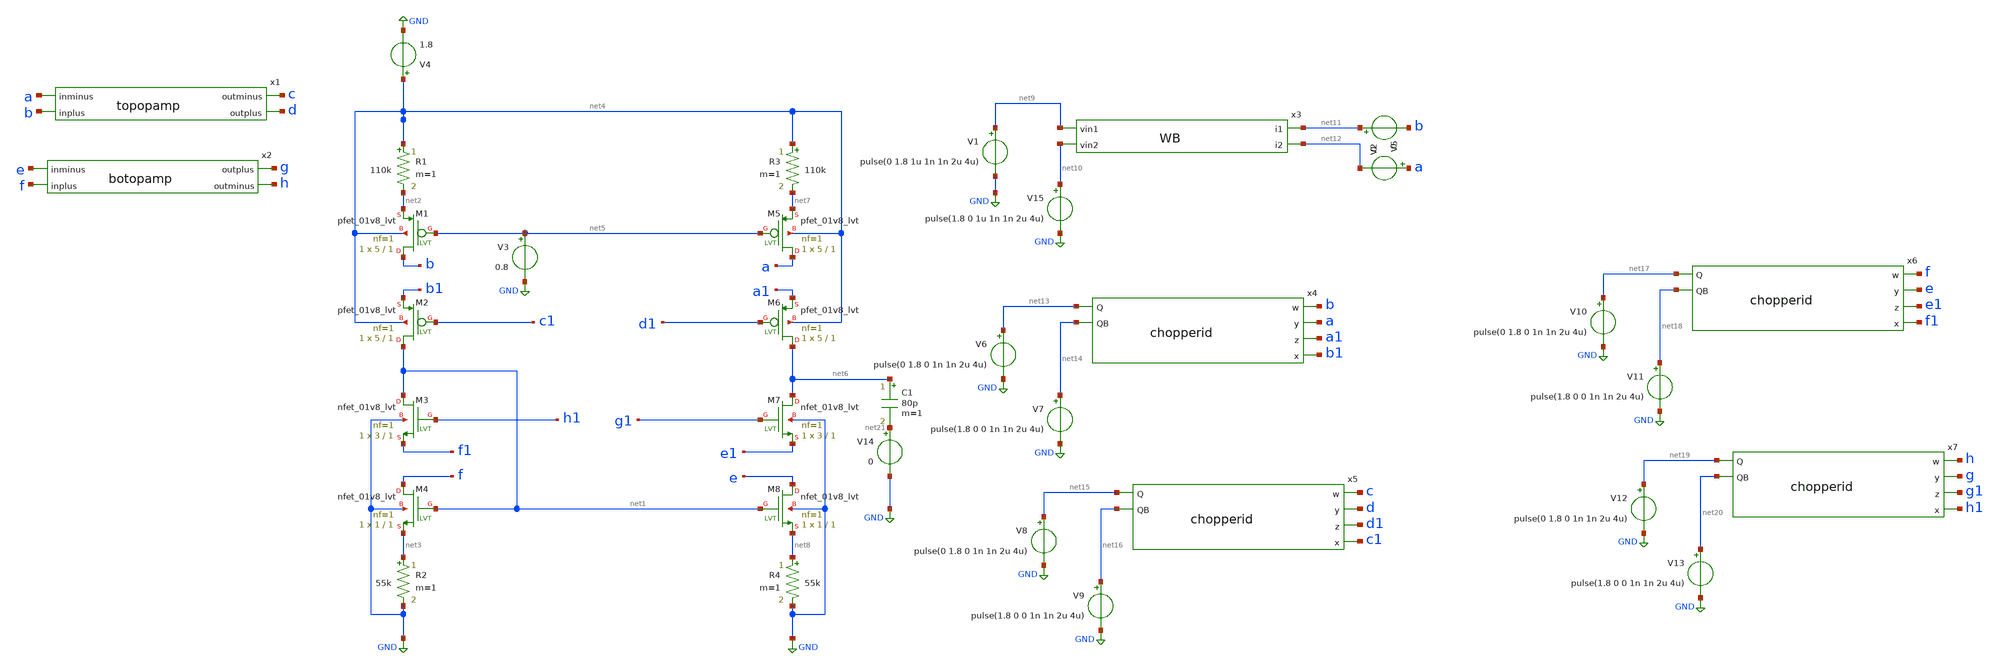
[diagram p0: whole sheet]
** sch_path: current_buffer.sch
**.subckt current_buffer
XM1 b net5 net2 net4 sky130_fd_pr__pfet_01v8_lvt L=1 W=5 nf=1 ad='int((nf+1)/2) * W/nf * 0.29' as='int((nf+2)/2) * W/nf * 0.29'
+ pd='2*int((nf+1)/2) * (W/nf + 0.29)' ps='2*int((nf+2)/2) * (W/nf + 0.29)' nrd='0.29 / W' nrs='0.29 / W'
+ sa=0 sb=0 sd=0 mult=1 m=1
XM2 net1 c1 b1 net4 sky130_fd_pr__pfet_01v8_lvt L=1 W=5 nf=1 ad='int((nf+1)/2) * W/nf * 0.29' as='int((nf+2)/2) * W/nf * 0.29'
+ pd='2*int((nf+1)/2) * (W/nf + 0.29)' ps='2*int((nf+2)/2) * (W/nf + 0.29)' nrd='0.29 / W' nrs='0.29 / W'
+ sa=0 sb=0 sd=0 mult=1 m=1
XM3 net1 h1 f1 GND sky130_fd_pr__nfet_01v8_lvt L=1 W=3 nf=1 ad='int((nf+1)/2) * W/nf * 0.29' as='int((nf+2)/2) * W/nf * 0.29'
+ pd='2*int((nf+1)/2) * (W/nf + 0.29)' ps='2*int((nf+2)/2) * (W/nf + 0.29)' nrd='0.29 / W' nrs='0.29 / W'
+ sa=0 sb=0 sd=0 mult=1 m=1
XM4 f net1 net3 GND sky130_fd_pr__nfet_01v8_lvt L=1 W=1 nf=1 ad='int((nf+1)/2) * W/nf * 0.29' as='int((nf+2)/2) * W/nf * 0.29'
+ pd='2*int((nf+1)/2) * (W/nf + 0.29)' ps='2*int((nf+2)/2) * (W/nf + 0.29)' nrd='0.29 / W' nrs='0.29 / W'
+ sa=0 sb=0 sd=0 mult=1 m=1
R1 net4 net2 110k m=1
R2 net3 GND 55k m=1
V3 net5 GND 0.8
V4 net4 GND 1.8
XM5 a net5 net7 net4 sky130_fd_pr__pfet_01v8_lvt L=1 W=5 nf=1 ad='int((nf+1)/2) * W/nf * 0.29' as='int((nf+2)/2) * W/nf * 0.29'
+ pd='2*int((nf+1)/2) * (W/nf + 0.29)' ps='2*int((nf+2)/2) * (W/nf + 0.29)' nrd='0.29 / W' nrs='0.29 / W'
+ sa=0 sb=0 sd=0 mult=1 m=1
XM6 net6 d1 a1 net4 sky130_fd_pr__pfet_01v8_lvt L=1 W=5 nf=1 ad='int((nf+1)/2) * W/nf * 0.29' as='int((nf+2)/2) * W/nf * 0.29'
+ pd='2*int((nf+1)/2) * (W/nf + 0.29)' ps='2*int((nf+2)/2) * (W/nf + 0.29)' nrd='0.29 / W' nrs='0.29 / W'
+ sa=0 sb=0 sd=0 mult=1 m=1
XM7 net6 g1 e1 GND sky130_fd_pr__nfet_01v8_lvt L=1 W=3 nf=1 ad='int((nf+1)/2) * W/nf * 0.29' as='int((nf+2)/2) * W/nf * 0.29'
+ pd='2*int((nf+1)/2) * (W/nf + 0.29)' ps='2*int((nf+2)/2) * (W/nf + 0.29)' nrd='0.29 / W' nrs='0.29 / W'
+ sa=0 sb=0 sd=0 mult=1 m=1
XM8 e net1 net8 GND sky130_fd_pr__nfet_01v8_lvt L=1 W=1 nf=1 ad='int((nf+1)/2) * W/nf * 0.29' as='int((nf+2)/2) * W/nf * 0.29'
+ pd='2*int((nf+1)/2) * (W/nf + 0.29)' ps='2*int((nf+2)/2) * (W/nf + 0.29)' nrd='0.29 / W' nrs='0.29 / W'
+ sa=0 sb=0 sd=0 mult=1 m=1
R3 net4 net7 110k m=1
R4 net8 GND 55k m=1
x1 a b c d topopamp
x2 g h e f botopamp
x3 net9 net11 net12 net10 WB
V1 net9 GND pulse(0 1.8 1u 1n 1n 2u 4u)
V2 net11 b 0
V5 a net12 0
x4 net13 b a net14 a1 b1 chopperid
V6 net13 GND pulse(0 1.8 0 1n 1n 2u 4u)
V7 net14 GND pulse(1.8 0 0 1n 1n 2u 4u)
x5 net15 c d net16 d1 c1 chopperid
V8 net15 GND pulse(0 1.8 0 1n 1n 2u 4u)
V9 net16 GND pulse(1.8 0 0 1n 1n 2u 4u)
x6 net17 f e net18 e1 f1 chopperid
V10 net17 GND pulse(0 1.8 0 1n 1n 2u 4u)
V11 net18 GND pulse(1.8 0 0 1n 1n 2u 4u)
x7 net19 h g net20 g1 h1 chopperid
V12 net19 GND pulse(0 1.8 0 1n 1n 2u 4u)
V13 net20 GND pulse(1.8 0 0 1n 1n 2u 4u)
C1 net6 net21 80p m=1
V14 net21 GND 0
V15 net10 GND pulse(1.8 0 1u 1n 1n 2u 4u)
**** begin user architecture code

.lib ~/open_pdks/sky130/sky130A/libs.tech/ngspice/sky130.lib.spice tt
.MODEL swmod SW(VT=0.9 VH=0 RON=1 ROFF=10000000000)


.tran 10n 50u
.control
save all
run
.endc

**** end user architecture code
**.ends
.GLOBAL GND
.end
